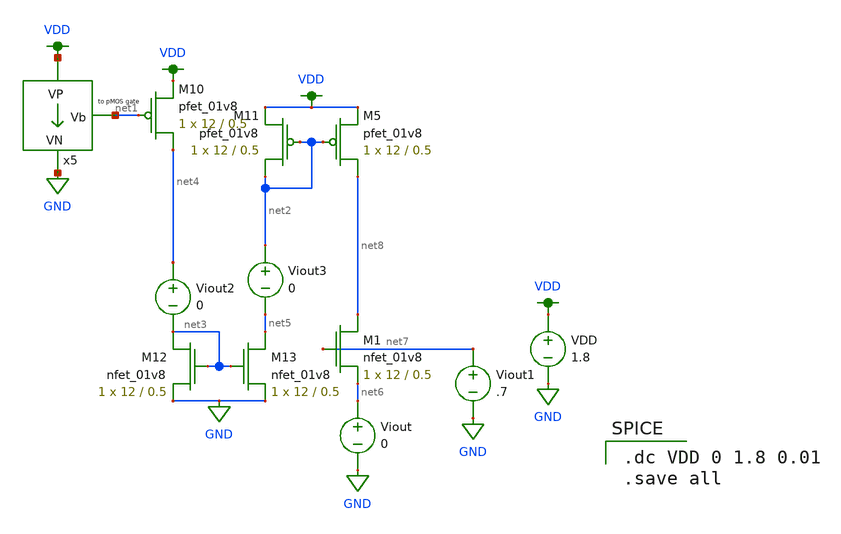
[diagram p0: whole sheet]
** sch_path: test.sch
**.subckt test
XM10 net4 net1 VDD VDD sky130_fd_pr__pfet_01v8 L=0.5 W=12 nf=1 ad='int((nf+1)/2) * W/nf * 0.29' as='int((nf+2)/2) * W/nf * 0.29'
+ pd='2*int((nf+1)/2) * (W/nf + 0.29)' ps='2*int((nf+2)/2) * (W/nf + 0.29)' nrd='0.29 / W' nrs='0.29 / W'
+ sa=0 sb=0 sd=0 mult=1 m=1
x5 VDD net1 GND current_bias
XM11 net2 net2 VDD VDD sky130_fd_pr__pfet_01v8 L=0.5 W=12 nf=1 ad='int((nf+1)/2) * W/nf * 0.29' as='int((nf+2)/2) * W/nf * 0.29'
+ pd='2*int((nf+1)/2) * (W/nf + 0.29)' ps='2*int((nf+2)/2) * (W/nf + 0.29)' nrd='0.29 / W' nrs='0.29 / W'
+ sa=0 sb=0 sd=0 mult=1 m=1
XM12 net3 net3 GND GND sky130_fd_pr__nfet_01v8 L=0.5 W=12 nf=1 ad='int((nf+1)/2) * W/nf * 0.29' as='int((nf+2)/2) * W/nf * 0.29'
+ pd='2*int((nf+1)/2) * (W/nf + 0.29)' ps='2*int((nf+2)/2) * (W/nf + 0.29)' nrd='0.29 / W' nrs='0.29 / W'
+ sa=0 sb=0 sd=0 mult=1 m=1
XM13 net5 net3 GND GND sky130_fd_pr__nfet_01v8 L=0.5 W=12 nf=1 ad='int((nf+1)/2) * W/nf * 0.29' as='int((nf+2)/2) * W/nf * 0.29'
+ pd='2*int((nf+1)/2) * (W/nf + 0.29)' ps='2*int((nf+2)/2) * (W/nf + 0.29)' nrd='0.29 / W' nrs='0.29 / W'
+ sa=0 sb=0 sd=0 mult=1 m=1
XM5 net8 net2 VDD VDD sky130_fd_pr__pfet_01v8 L=0.5 W=12 nf=1 ad='int((nf+1)/2) * W/nf * 0.29' as='int((nf+2)/2) * W/nf * 0.29'
+ pd='2*int((nf+1)/2) * (W/nf + 0.29)' ps='2*int((nf+2)/2) * (W/nf + 0.29)' nrd='0.29 / W' nrs='0.29 / W'
+ sa=0 sb=0 sd=0 mult=1 m=1
Viout net6 GND 0
VDD VDD GND 1.8
XM1 net8 net7 net6 GND sky130_fd_pr__nfet_01v8 L=0.5 W=12 nf=1 ad='int((nf+1)/2) * W/nf * 0.29' as='int((nf+2)/2) * W/nf * 0.29'
+ pd='2*int((nf+1)/2) * (W/nf + 0.29)' ps='2*int((nf+2)/2) * (W/nf + 0.29)' nrd='0.29 / W' nrs='0.29 / W'
+ sa=0 sb=0 sd=0 mult=1 m=1
Viout1 net7 GND .7
Viout2 net4 net3 0
Viout3 net2 net5 0
**** begin user architecture code

.option wnflag=1
.param MC_SWITCH=0.0
.lib ~/skywater/skywater-pdk/libraries/sky130_fd_pr_ngspice/latest/models/sky130.lib.spice tt


.dc VDD 0 1.8 0.01
.save all

**** end user architecture code
**.ends
.GLOBAL VDD
.GLOBAL GND
.end
